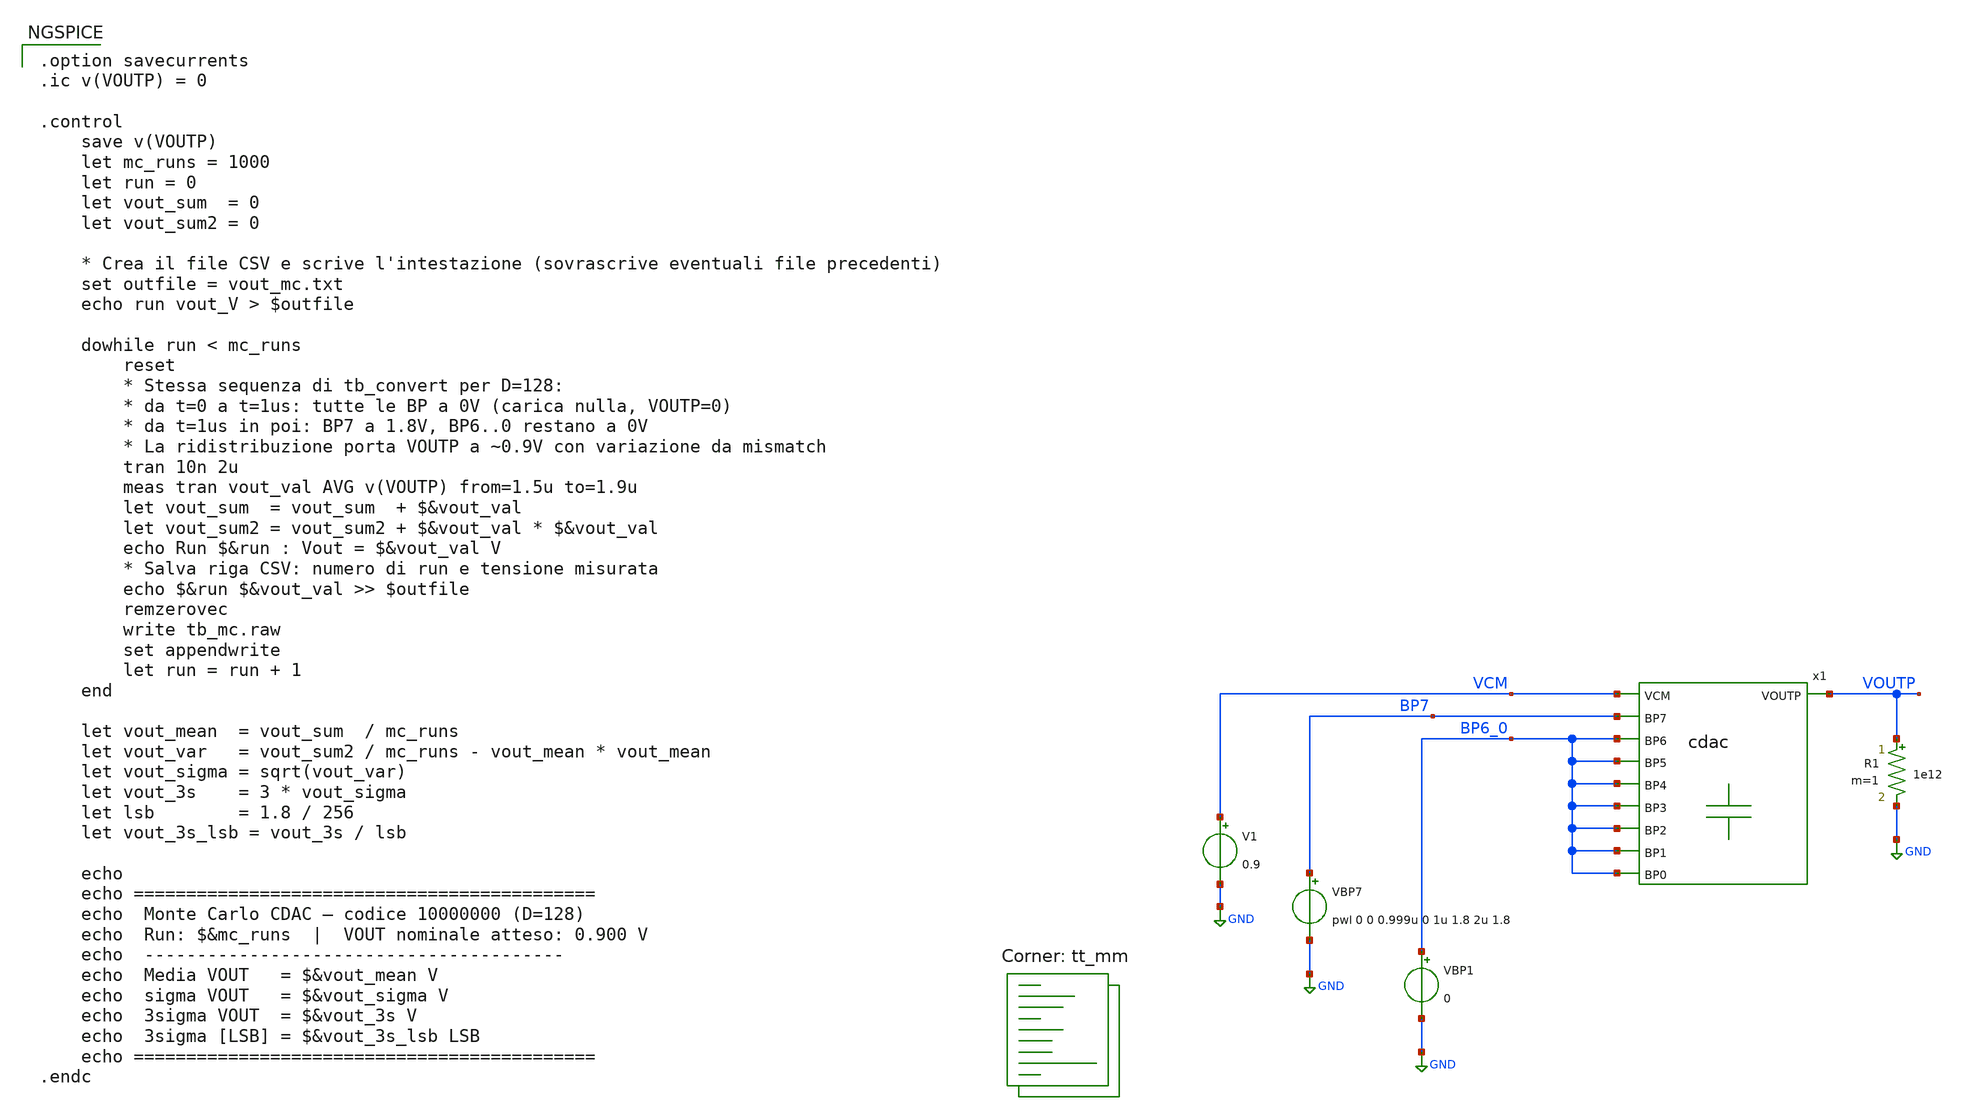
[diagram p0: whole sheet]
** sch_path: 02_sky130_pdk/soluzioni/lab_cdac/xschem/tb_mc.sch
**.subckt tb_mc
VBP7 BP7 GND pwl 0 0 0.999u 0 1u 1.8 2u 1.8
VBP1 BP6_0 GND 0
x1 VOUTP VCM BP6_0 BP6_0 BP6_0 BP6_0 BP6_0 BP6_0 BP7 BP6_0 cdac
V1 VCM GND 0.9
R1 VOUTP GND 1e12 m=1
**** begin user architecture code

.option savecurrents
.ic v(VOUTP) = 0

.control
    save v(VOUTP)
    let mc_runs = 1000
    let run = 0
    let vout_sum  = 0
    let vout_sum2 = 0

    * Crea il file CSV e scrive l'intestazione (sovrascrive eventuali file precedenti)
    set outfile = vout_mc.txt
    echo run vout_V > $outfile

    dowhile run < mc_runs
        reset
        * Stessa sequenza di tb_convert per D=128:
        * da t=0 a t=1us: tutte le BP a 0V (carica nulla, VOUTP=0)
        * da t=1us in poi: BP7 a 1.8V, BP6..0 restano a 0V
        * La ridistribuzione porta VOUTP a ~0.9V con variazione da mismatch
        tran 10n 2u
        meas tran vout_val AVG v(VOUTP) from=1.5u to=1.9u
        let vout_sum  = vout_sum  + $&vout_val
        let vout_sum2 = vout_sum2 + $&vout_val * $&vout_val
        echo Run $&run : Vout = $&vout_val V
        * Salva riga CSV: numero di run e tensione misurata
        echo $&run $&vout_val >> $outfile
        remzerovec
        write tb_mc.raw
        set appendwrite
        let run = run + 1
    end

    let vout_mean  = vout_sum  / mc_runs
    let vout_var   = vout_sum2 / mc_runs - vout_mean * vout_mean
    let vout_sigma = sqrt(vout_var)
    let vout_3s    = 3 * vout_sigma
    let lsb        = 1.8 / 256
    let vout_3s_lsb = vout_3s / lsb

    echo
    echo ============================================
    echo  Monte Carlo CDAC — codice 10000000 (D=128)
    echo  Run: $&mc_runs  |  VOUT nominale atteso: 0.900 V
    echo  ----------------------------------------
    echo  Media VOUT   = $&vout_mean V
    echo  sigma VOUT   = $&vout_sigma V
    echo  3sigma VOUT  = $&vout_3s V
    echo  3sigma [LSB] = $&vout_3s_lsb LSB
    echo ============================================
.endc

.lib $::SKYWATER_MODELS/sky130.lib.spice tt_mm
**** end user architecture code
**.ends

* expanding   symbol:  cdac.sym # of pins=10
** sym_path: 02_sky130_pdk/soluzioni/lab_cdac/xschem/cdac.sym
** sch_path: 02_sky130_pdk/soluzioni/lab_cdac/xschem/cdac.sch
.subckt cdac VOUTP VCM BP3 BP2 BP5 BP4 BP1 BP6 BP7 BP0
*.ipin VCM
*.opin VOUTP
*.ipin BP0
*.ipin BP1
*.ipin BP2
*.ipin BP3
*.ipin BP4
*.ipin BP5
*.ipin BP6
*.ipin BP7
XC1 VCM VOUTP sky130_fd_pr__cap_mim_m3_1 W=5 L=5 MF=1 m=1
XC2 BP0 VOUTP sky130_fd_pr__cap_mim_m3_1 W=5 L=5 MF=1 m=1
XC3 BP1 VOUTP sky130_fd_pr__cap_mim_m3_1 W=5 L=5 MF=2 m=2
XC4 BP2 VOUTP sky130_fd_pr__cap_mim_m3_1 W=5 L=5 MF=4 m=4
XC5 BP3 VOUTP sky130_fd_pr__cap_mim_m3_1 W=5 L=5 MF=8 m=8
XC6 BP4 VOUTP sky130_fd_pr__cap_mim_m3_1 W=5 L=5 MF=16 m=16
XC7 BP5 VOUTP sky130_fd_pr__cap_mim_m3_1 W=5 L=5 MF=32 m=32
XC8 BP6 VOUTP sky130_fd_pr__cap_mim_m3_1 W=5 L=5 MF=64 m=64
XC9 BP7 VOUTP sky130_fd_pr__cap_mim_m3_1 W=5 L=5 MF=128 m=128
.ends

.GLOBAL GND
.end
